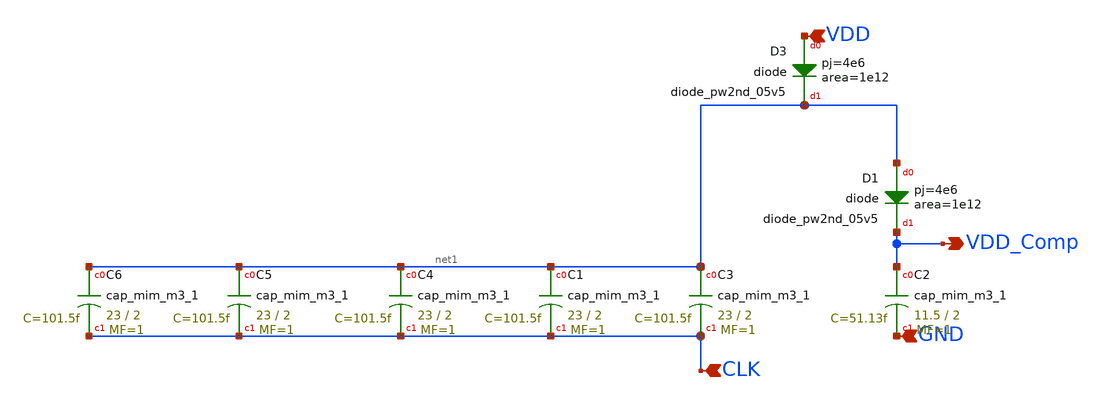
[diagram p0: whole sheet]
** sch_path: xschem/schematic_lvs/voltage_doubler.sch
**.subckt voltage_doubler CLK VDD_Comp VDD GND
*.ipin CLK
*.opin VDD_Comp
*.ipin VDD
*.ipin GND
XD1 net1 VDD_Comp sky130_fd_pr__diode_pw2nd_05v5 area=1e12 pj=4e6
XD3 VDD net1 sky130_fd_pr__diode_pw2nd_05v5 area=1e12 pj=4e6
XC2 VDD_Comp GND sky130_fd_pr__cap_mim_m3_1 W=11.5 L=2 MF=1 m=1
XC3 net1 CLK sky130_fd_pr__cap_mim_m3_1 W=23 L=2 MF=1 m=1
XC1 net1 CLK sky130_fd_pr__cap_mim_m3_1 W=23 L=2 MF=1 m=1
XC4 net1 CLK sky130_fd_pr__cap_mim_m3_1 W=23 L=2 MF=1 m=1
XC5 net1 CLK sky130_fd_pr__cap_mim_m3_1 W=23 L=2 MF=1 m=1
XC6 net1 CLK sky130_fd_pr__cap_mim_m3_1 W=23 L=2 MF=1 m=1
**.ends
.end
